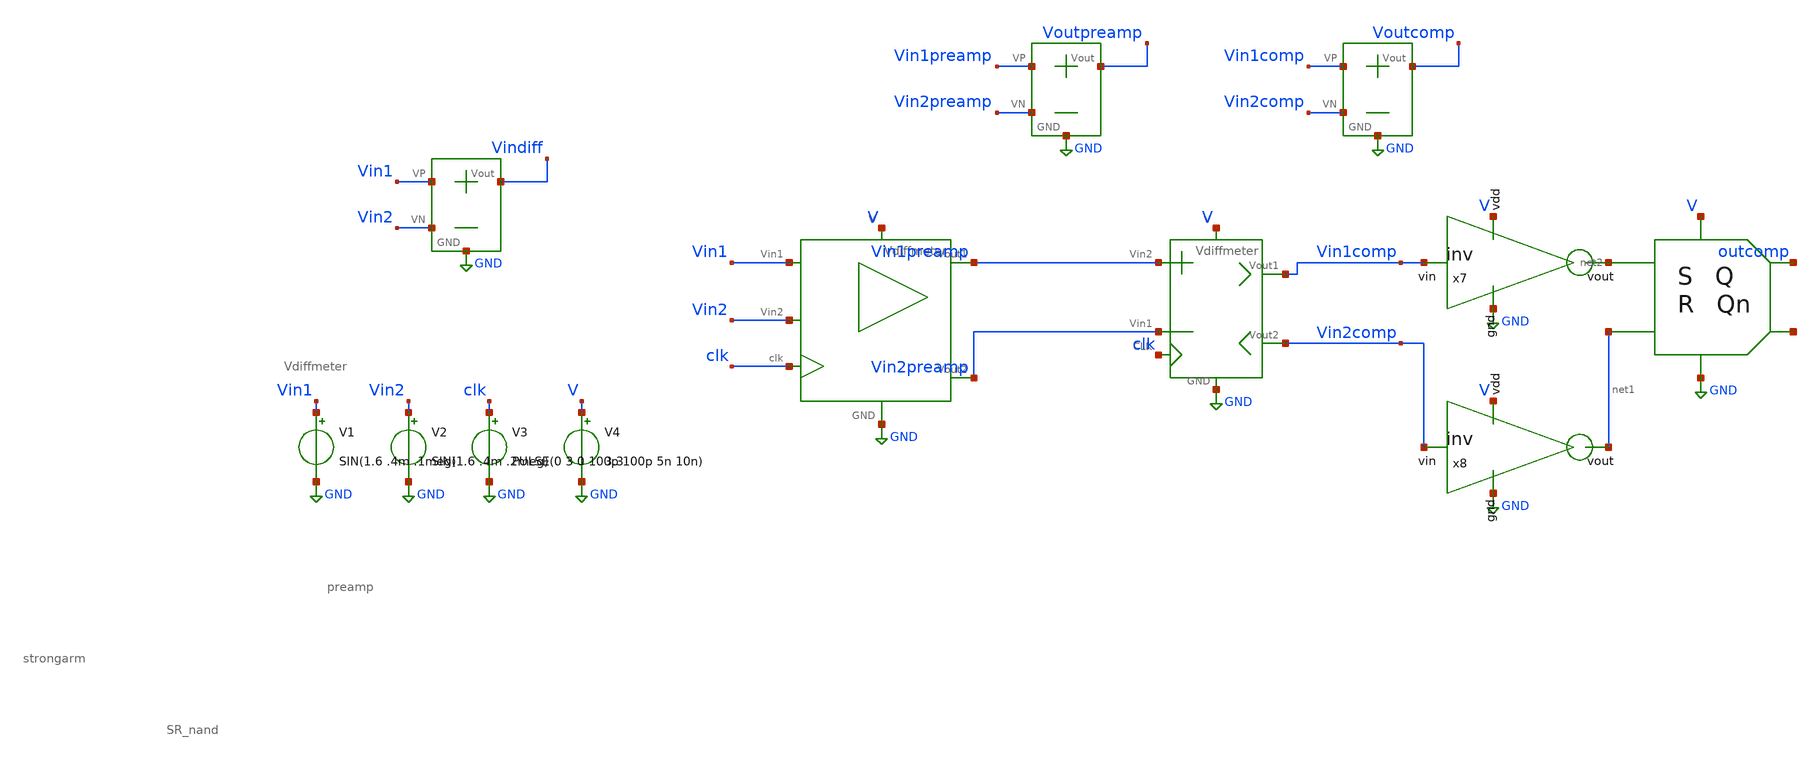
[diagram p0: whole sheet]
** sch_path: SAR_ADC/xschem/test/comp_full_tb/no_symbol/sin_1meg-sin_2meg-nandlatch__tb.sch
**.subckt sin_1meg-sin_2meg-nandlatch__tb
X3 V GND Vin1 clk Vin1preamp Vin2preamp Vin2 preamp
X4 V GND Vin2preamp Vin1preamp clk Vin1comp Vin2comp strongarm
V1 Vin1 GND SIN(1.6 .4m .1meg)
V2 Vin2 GND SIN(1.6 .4m .2meg)
V3 clk GND PULSE(0 3 0 100p 100p 5n 10n)
V4 V GND 3.3
X5 Vin1 Vin2 Vindiff GND Vdiffmeter
X2 Vin1preamp Vin2preamp Voutpreamp GND Vdiffmeter
X6 Vin1comp Vin2comp Voutcomp GND Vdiffmeter
X1 net2 V GND net1 outcomp net3 SR_nand
x7 V GND net2 Vin1comp inv cl=0.28u wp=0.44u wn=0.22u
x8 V GND net1 Vin2comp inv cl=0.28u wp=0.44u wn=0.22u
**** begin user architecture code


.control
save all
tran 500p 20u
plot vindiff outcomp
plot vindiff Voutpreamp
plot Voutpreamp Voutcomp
plot outcomp Voutcomp
plot {vindiff * 1000} voutcomp
plot {vindiff * 1000} outcomp
.endc


.include /foss/pdks/gf180mcuC/libs.tech/ngspice/design.ngspice
.lib /foss/pdks/gf180mcuC/libs.tech/ngspice/sm141064.ngspice typical

**** end user architecture code
**.ends
.GLOBAL GND
.end
